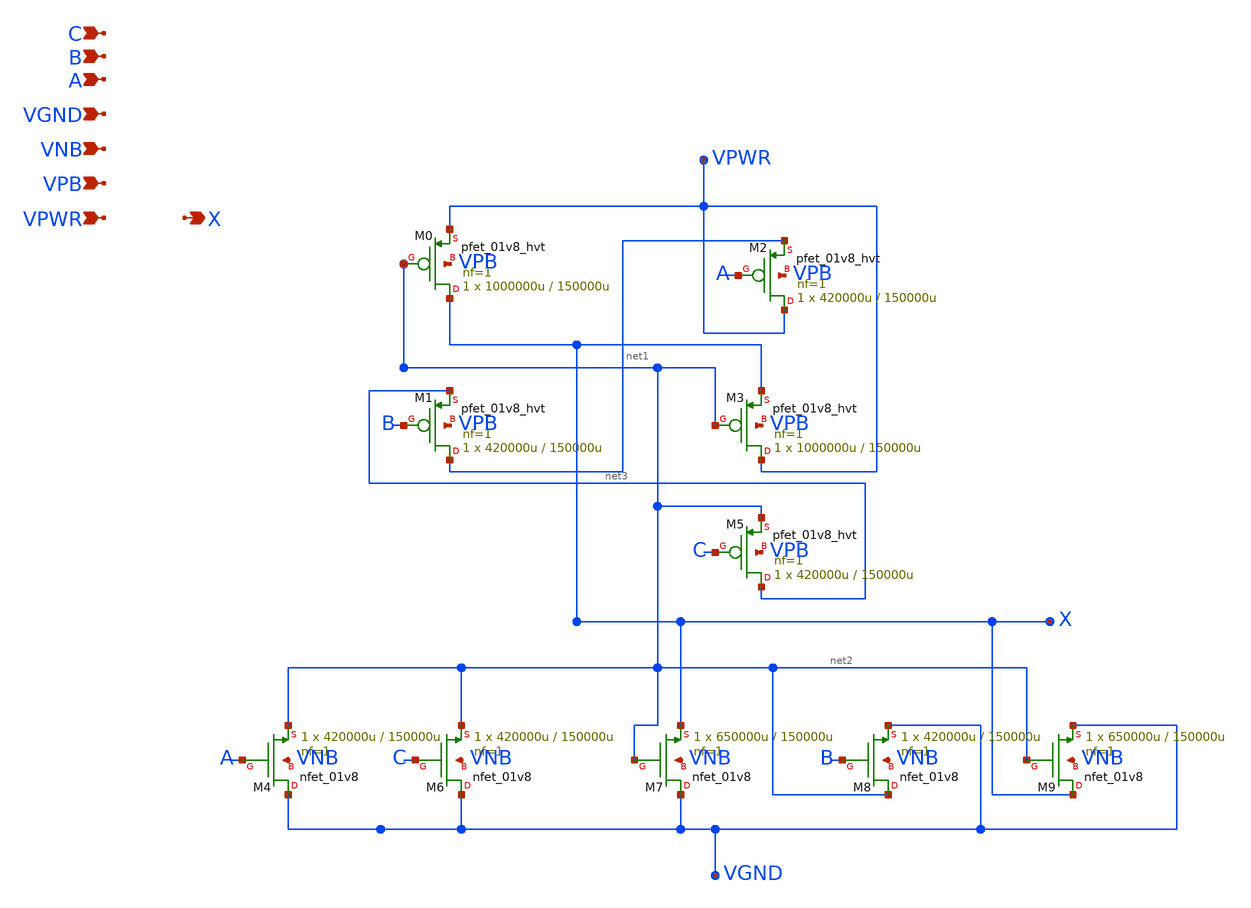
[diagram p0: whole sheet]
** sch_path: schematics/or3/sky130_fd_sc_hd__or3_2.sch
**.subckt sky130_fd_sc_hd__or3_2 A B C VGND VNB VPB VPWR X
*.ipin A
*.ipin B
*.ipin C
*.ipin VGND
*.ipin VNB
*.ipin VPB
*.ipin VPWR
*.opin X
XM0 X net2 VPWR VPB sky130_fd_pr__pfet_01v8_hvt L=150000u W=1000000u nf=1 ad='int((nf+1)/2) * W/nf * 0.29'
+ as='int((nf+2)/2) * W/nf * 0.29' pd='2*int((nf+1)/2) * (W/nf + 0.29)' ps='2*int((nf+2)/2) * (W/nf + 0.29)'
+ nrd='0.29 / W' nrs='0.29 / W' sa=0 sb=0 sd=0 mult=1 m=1
XM2 VPWR A net1 VPB sky130_fd_pr__pfet_01v8_hvt L=150000u W=420000u nf=1 ad='int((nf+1)/2) * W/nf * 0.29'
+ as='int((nf+2)/2) * W/nf * 0.29' pd='2*int((nf+1)/2) * (W/nf + 0.29)' ps='2*int((nf+2)/2) * (W/nf + 0.29)'
+ nrd='0.29 / W' nrs='0.29 / W' sa=0 sb=0 sd=0 mult=1 m=1
XM1 net1 B net3 VPB sky130_fd_pr__pfet_01v8_hvt L=150000u W=420000u nf=1 ad='int((nf+1)/2) * W/nf * 0.29'
+ as='int((nf+2)/2) * W/nf * 0.29' pd='2*int((nf+1)/2) * (W/nf + 0.29)' ps='2*int((nf+2)/2) * (W/nf + 0.29)'
+ nrd='0.29 / W' nrs='0.29 / W' sa=0 sb=0 sd=0 mult=1 m=1
XM3 VPWR net2 X VPB sky130_fd_pr__pfet_01v8_hvt L=150000u W=1000000u nf=1 ad='int((nf+1)/2) * W/nf * 0.29'
+ as='int((nf+2)/2) * W/nf * 0.29' pd='2*int((nf+1)/2) * (W/nf + 0.29)' ps='2*int((nf+2)/2) * (W/nf + 0.29)'
+ nrd='0.29 / W' nrs='0.29 / W' sa=0 sb=0 sd=0 mult=1 m=1
XM5 net3 C net2 VPB sky130_fd_pr__pfet_01v8_hvt L=150000u W=420000u nf=1 ad='int((nf+1)/2) * W/nf * 0.29'
+ as='int((nf+2)/2) * W/nf * 0.29' pd='2*int((nf+1)/2) * (W/nf + 0.29)' ps='2*int((nf+2)/2) * (W/nf + 0.29)'
+ nrd='0.29 / W' nrs='0.29 / W' sa=0 sb=0 sd=0 mult=1 m=1
XM4 VGND A net2 VNB sky130_fd_pr__nfet_01v8 L=150000u W=420000u nf=1 ad='int((1 + 1)/2) * 420000u / 1 * 0.29'
+ as='int((1 + 2)/2) * 420000u / 1 * 0.29' pd='2*int((1 + 1)/2) * (420000u / 1 + 0.29)' ps='2*int((1 + 2)/2) * (420000u / 1 + 0.29)'
+ nrd='0.29 / 420000u ' nrs='0.29 / 420000u ' sa=0 sb=0 sd=0 mult=1 m=1
XM6 VGND C net2 VNB sky130_fd_pr__nfet_01v8 L=150000u W=420000u nf=1 ad='int((1 + 1)/2) * 420000u / 1 * 0.29'
+ as='int((1 + 2)/2) * 420000u / 1 * 0.29' pd='2*int((1 + 1)/2) * (420000u / 1 + 0.29)' ps='2*int((1 + 2)/2) * (420000u / 1 + 0.29)'
+ nrd='0.29 / 420000u ' nrs='0.29 / 420000u ' sa=0 sb=0 sd=0 mult=1 m=1
XM7 VGND net2 X VNB sky130_fd_pr__nfet_01v8 L=150000u W=650000u nf=1 ad='int((1 + 1)/2) * 650000u / 1 * 0.29'
+ as='int((1 + 2)/2) * 650000u / 1 * 0.29' pd='2*int((1 + 1)/2) * (650000u / 1 + 0.29)' ps='2*int((1 + 2)/2) * (650000u / 1 + 0.29)'
+ nrd='0.29 / 650000u ' nrs='0.29 / 650000u ' sa=0 sb=0 sd=0 mult=1 m=1
XM8 net2 B VGND VNB sky130_fd_pr__nfet_01v8 L=150000u W=420000u nf=1 ad='int((1 + 1)/2) * 420000u / 1 * 0.29'
+ as='int((1 + 2)/2) * 420000u / 1 * 0.29' pd='2*int((1 + 1)/2) * (420000u / 1 + 0.29)' ps='2*int((1 + 2)/2) * (420000u / 1 + 0.29)'
+ nrd='0.29 / 420000u ' nrs='0.29 / 420000u ' sa=0 sb=0 sd=0 mult=1 m=1
XM9 X net2 VGND VNB sky130_fd_pr__nfet_01v8 L=150000u W=650000u nf=1 ad='int((1 + 1)/2) * 650000u / 1 * 0.29'
+ as='int((1 + 2)/2) * 650000u / 1 * 0.29' pd='2*int((1 + 1)/2) * (650000u / 1 + 0.29)' ps='2*int((1 + 2)/2) * (650000u / 1 + 0.29)'
+ nrd='0.29 / 650000u ' nrs='0.29 / 650000u ' sa=0 sb=0 sd=0 mult=1 m=1
**.ends
.end
